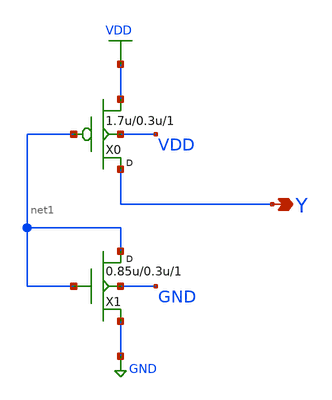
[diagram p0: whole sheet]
** sch_path: lib/xschem/gf180mcu_osu_sc_12T_tiehi.sch
**.subckt gf180mcu_osu_sc_12T_tiehi Y
*.opin Y
X0 Y net1 VDD VDD pmos_3p3 w=1.7u l=0.3u m=1
X1 net1 net1 GND GND nmos_3p3 w=0.85u l=0.3u m=1
**** begin user architecture code


.inc "/import/yukari1/lrburle/OSU_180/char/techfiles/design.hspice"
.lib "/import/yukari1/lrburle/OSU_180/char/techfiles/sm141064.hspice" typical


**** end user architecture code
**.ends
.GLOBAL VDD
.GLOBAL GND
.end
